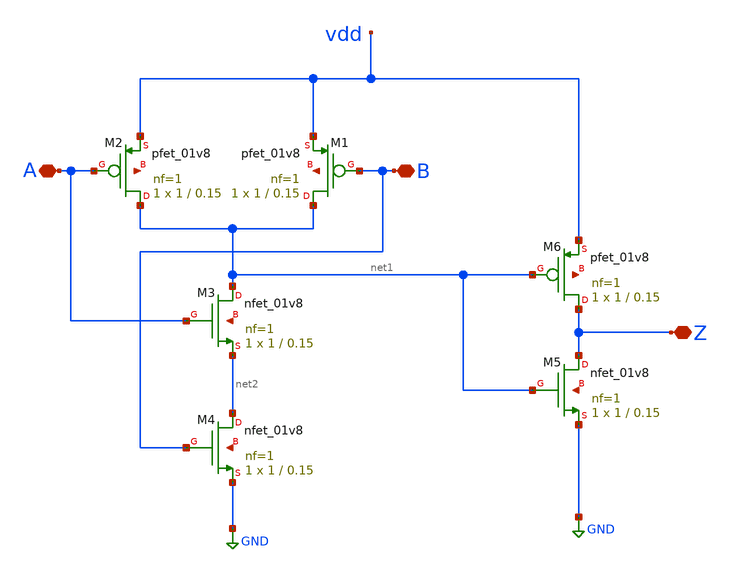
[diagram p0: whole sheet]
** sch_path: sch/and.sch
**.subckt and A B Z
*.iopin A
*.iopin B
*.iopin Z
XM1 net1 B vdd net3 sky130_fd_pr__pfet_01v8 L=0.15 W=1 nf=1 ad='int((nf+1)/2) * W/nf * 0.29' as='int((nf+2)/2) * W/nf * 0.29'
+ pd='2*int((nf+1)/2) * (W/nf + 0.29)' ps='2*int((nf+2)/2) * (W/nf + 0.29)' nrd='0.29 / W' nrs='0.29 / W'
+ sa=0 sb=0 sd=0 mult=1 m=1
XM2 net1 A vdd net4 sky130_fd_pr__pfet_01v8 L=0.15 W=1 nf=1 ad='int((nf+1)/2) * W/nf * 0.29' as='int((nf+2)/2) * W/nf * 0.29'
+ pd='2*int((nf+1)/2) * (W/nf + 0.29)' ps='2*int((nf+2)/2) * (W/nf + 0.29)' nrd='0.29 / W' nrs='0.29 / W'
+ sa=0 sb=0 sd=0 mult=1 m=1
XM3 net1 A net2 net5 sky130_fd_pr__nfet_01v8 L=0.15 W=1 nf=1 ad='int((nf+1)/2) * W/nf * 0.29' as='int((nf+2)/2) * W/nf * 0.29'
+ pd='2*int((nf+1)/2) * (W/nf + 0.29)' ps='2*int((nf+2)/2) * (W/nf + 0.29)' nrd='0.29 / W' nrs='0.29 / W'
+ sa=0 sb=0 sd=0 mult=1 m=1
XM4 net2 B GND net6 sky130_fd_pr__nfet_01v8 L=0.15 W=1 nf=1 ad='int((nf+1)/2) * W/nf * 0.29' as='int((nf+2)/2) * W/nf * 0.29'
+ pd='2*int((nf+1)/2) * (W/nf + 0.29)' ps='2*int((nf+2)/2) * (W/nf + 0.29)' nrd='0.29 / W' nrs='0.29 / W'
+ sa=0 sb=0 sd=0 mult=1 m=1
XM5 Z net1 GND net7 sky130_fd_pr__nfet_01v8 L=0.15 W=1 nf=1 ad='int((nf+1)/2) * W/nf * 0.29' as='int((nf+2)/2) * W/nf * 0.29'
+ pd='2*int((nf+1)/2) * (W/nf + 0.29)' ps='2*int((nf+2)/2) * (W/nf + 0.29)' nrd='0.29 / W' nrs='0.29 / W'
+ sa=0 sb=0 sd=0 mult=1 m=1
XM6 Z net1 vdd net8 sky130_fd_pr__pfet_01v8 L=0.15 W=1 nf=1 ad='int((nf+1)/2) * W/nf * 0.29' as='int((nf+2)/2) * W/nf * 0.29'
+ pd='2*int((nf+1)/2) * (W/nf + 0.29)' ps='2*int((nf+2)/2) * (W/nf + 0.29)' nrd='0.29 / W' nrs='0.29 / W'
+ sa=0 sb=0 sd=0 mult=1 m=1
**.ends
.GLOBAL GND
.end
